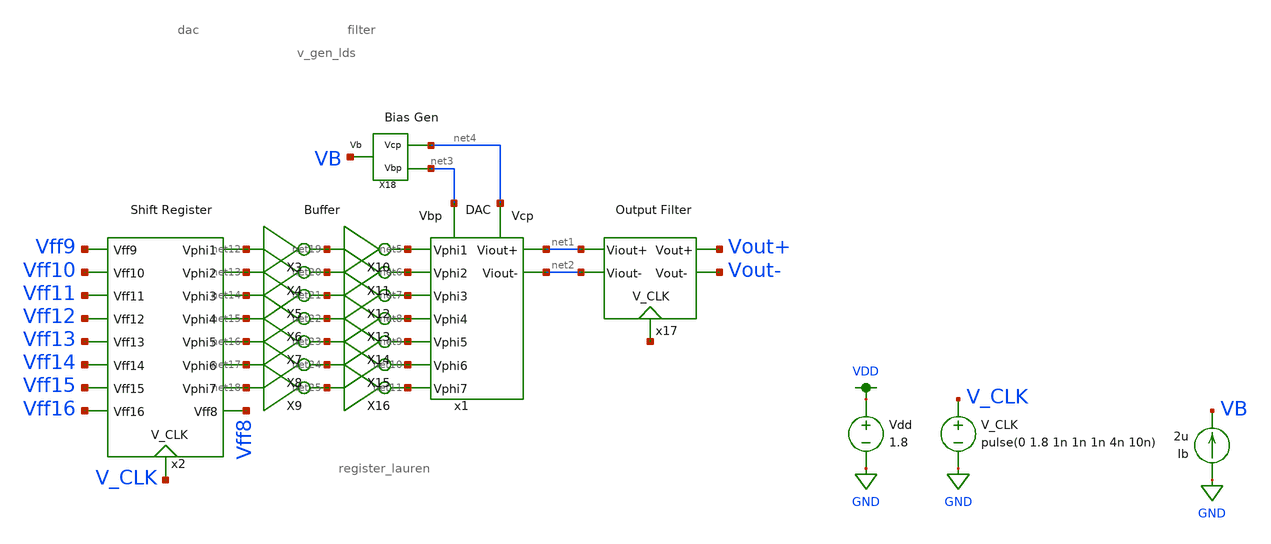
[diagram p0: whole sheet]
** sch_path: simulation/register_dac_pres_andrew.sch
**.subckt register_dac_pres_andrew
V_CLK V_CLK GND pulse(0 1.8 1n 1n 1n 4n 10n)
Vdd VDD GND 1.8
x1 net5 net6 net7 net8 net9 net10 net11 net1 net2 net3 net4 dac
x2 Vff10 Vff11 Vff12 Vff13 Vff14 Vff16 Vff15 Vff9 net12 net13 net14 net15 net16 net17 net18 Vff8
+ V_CLK register_lauren
X3 net12 net19 inverter
X4 net13 net20 inverter
X5 net14 net21 inverter
X6 net15 net22 inverter
X7 net16 net23 inverter
X8 net17 net24 inverter
X9 net18 net25 inverter
X10 net19 net5 inverter
X11 net20 net6 inverter
X12 net21 net7 inverter
X13 net22 net8 inverter
X14 net23 net9 inverter
X15 net24 net10 inverter
X16 net25 net11 inverter
x17 net1 net2 Vout+ Vout- net26 filter
X18 net4 net3 VB v_gen_lds
Ib GND VB 2u
**** begin user architecture code

.option wnflag=1
.param MC_SWITCH=0.0
.lib ~/skywater/skywater-pdk/libraries/sky130_fd_pr_ngspice/latest/models/sky130.lib.spice tt


.ic v(phi1)=0 v(phi2)=0 v(phi3)=0 v(phi4)=0 v(phi5)=0 v(phi6)=0 v(phi7)=0 v(Vff8)=0 v(Vff9)=1.8
+ v(Vff10)=1.8 v(Vff11)=1.8 v(Vff12)=1.8 v(Vff13)=1.8 v(Vff14)=1.8 v(Vff15)=1.8 v(Vff16)=1.8
.tran 0.01n 1u
.save v(phi1f), v(phi2f), v(phi3f), v(phi4f), v(phi5f), v(phi6f), v(phi7f)

**** end user architecture code
**.ends
.GLOBAL GND
.GLOBAL VDD
.end
